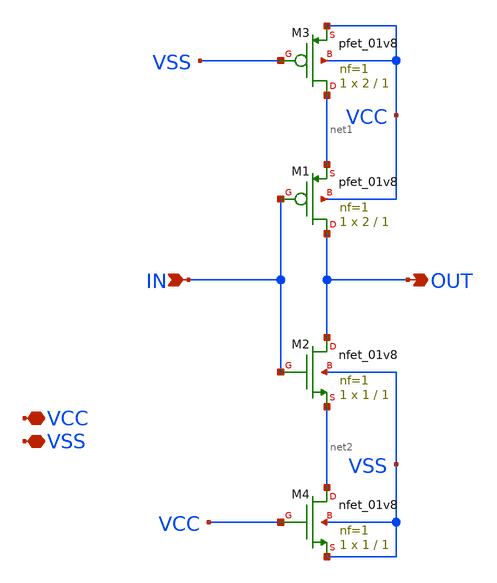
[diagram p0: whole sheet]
** sch_path: xschem/inverter.sch
**.subckt inverter VCC VSS IN OUT
*.iopin VCC
*.iopin VSS
*.ipin IN
*.opin OUT
XM1 OUT IN net1 VCC sky130_fd_pr__pfet_01v8 L=1 W=2 nf=1 ad='int((nf+1)/2) * W/nf * 0.29' as='int((nf+2)/2) * W/nf * 0.29'
+ pd='2*int((nf+1)/2) * (W/nf + 0.29)' ps='2*int((nf+2)/2) * (W/nf + 0.29)' nrd='0.29 / W' nrs='0.29 / W'
+ sa=0 sb=0 sd=0 mult=1 m=1
XM2 OUT IN net2 VSS sky130_fd_pr__nfet_01v8 L=1 W=1 nf=1 ad='int((nf+1)/2) * W/nf * 0.29' as='int((nf+2)/2) * W/nf * 0.29'
+ pd='2*int((nf+1)/2) * (W/nf + 0.29)' ps='2*int((nf+2)/2) * (W/nf + 0.29)' nrd='0.29 / W' nrs='0.29 / W'
+ sa=0 sb=0 sd=0 mult=1 m=1
XM3 net1 VSS VCC VCC sky130_fd_pr__pfet_01v8 L=1 W=2 nf=1 ad='int((nf+1)/2) * W/nf * 0.29' as='int((nf+2)/2) * W/nf * 0.29'
+ pd='2*int((nf+1)/2) * (W/nf + 0.29)' ps='2*int((nf+2)/2) * (W/nf + 0.29)' nrd='0.29 / W' nrs='0.29 / W'
+ sa=0 sb=0 sd=0 mult=1 m=1
XM4 net2 VCC VSS VSS sky130_fd_pr__nfet_01v8 L=1 W=1 nf=1 ad='int((nf+1)/2) * W/nf * 0.29' as='int((nf+2)/2) * W/nf * 0.29'
+ pd='2*int((nf+1)/2) * (W/nf + 0.29)' ps='2*int((nf+2)/2) * (W/nf + 0.29)' nrd='0.29 / W' nrs='0.29 / W'
+ sa=0 sb=0 sd=0 mult=1 m=1
**.ends
.end
